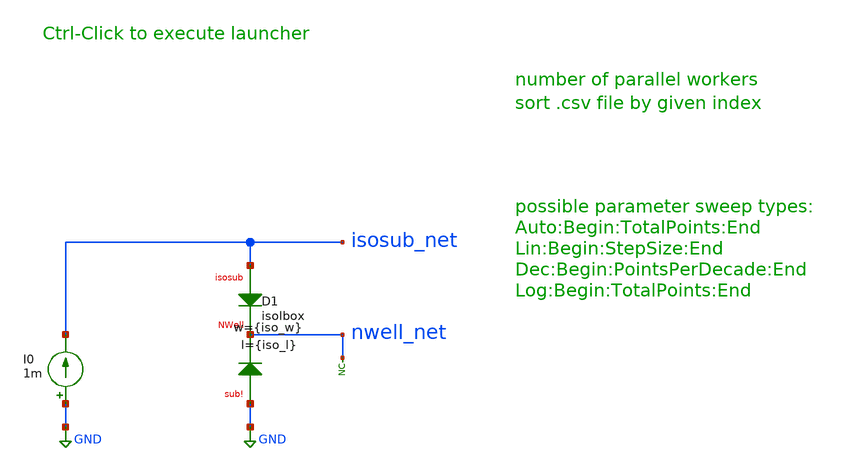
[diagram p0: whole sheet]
** sch_path: ihp-sg13g2/xschem_libs/sg13g2_tests_ase/isolbox_sweep_tb/schematic/isolbox_sweep_tb.sch
**.subckt isolbox_sweep_tb
I0 GND isosub_net 1m
XD1 isosub_net nwell_net GND isolbox l={iso_l} w={iso_w}
* noconn nwell_net
**.ends
.GLOBAL GND
.end
